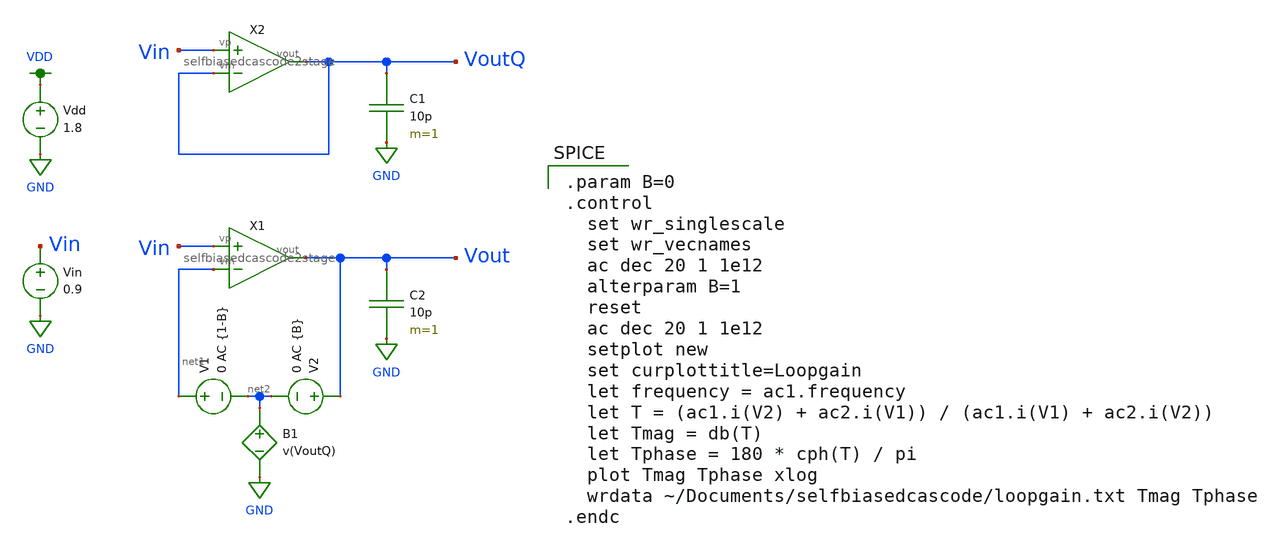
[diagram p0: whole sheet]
** sch_path: Final DAC files/schematics/opamp/selfbiasedcascode2stage_loopgain.sch
**.subckt selfbiasedcascode2stage_loopgain
Vdd VDD GND 1.8
Vin Vin GND 0.9
V1 net1 net2 0 AC {1-B}
V2 Vout net2 0 AC {B}
B1 net2 GND V=v(VoutQ)
X1 Vin net1 Vout selfbiasedcascode2stage
X2 Vin VoutQ VoutQ selfbiasedcascode2stage
C1 VoutQ GND 10p m=1
C2 Vout GND 10p m=1
**** begin user architecture code

.param B=0
.control
  set wr_singlescale
  set wr_vecnames
  ac dec 20 1 1e12
  alterparam B=1
  reset
  ac dec 20 1 1e12
  setplot new
  set curplottitle=Loopgain
  let frequency = ac1.frequency
  let T = (ac1.i(V2) + ac2.i(V1)) / (ac1.i(V1) + ac2.i(V2))
  let Tmag = db(T)
  let Tphase = 180 * cph(T) / pi
  plot Tmag Tphase xlog
  wrdata ~/Documents/selfbiasedcascode/loopgain.txt Tmag Tphase
.endc


.option wnflag=1
.param MC_SWITCH=0.0
.lib ~/skywater/skywater-pdk/libraries/sky130_fd_pr_ngspice/latest/models/sky130.lib.spice tt

**** end user architecture code
**.ends

* expanding   symbol:  /home/madvlsi/Documents/selfbiasedcascode/selfbiasedcascode2stage.sym # of
*+ pins=3
** sym_path: Final DAC files/schematics/opamp/selfbiasedcascode2stage.sym
** sch_path: Final DAC files/schematics/opamp/selfbiasedcascode2stage.sch
.subckt selfbiasedcascode2stage vp vm vout
*.ipin vp
*.ipin vm
*.opin vout
XM1 net11 net1 GND GND sky130_fd_pr__nfet_01v8 L=0.6 W=3 nf=1 ad='int((nf+1)/2) * W/nf * 0.29' as='int((nf+2)/2) * W/nf * 0.29'
+ pd='2*int((nf+1)/2) * (W/nf + 0.29)' ps='2*int((nf+2)/2) * (W/nf + 0.29)' nrd='0.29 / W' nrs='0.29 / W'
+ sa=0 sb=0 sd=0 mult=1 m=1
XM9 net12 net3 VDD VDD sky130_fd_pr__pfet_01v8 L=0.6 W=3 nf=1 ad='int((nf+1)/2) * W/nf * 0.29' as='int((nf+2)/2) * W/nf * 0.29'
+ pd='2*int((nf+1)/2) * (W/nf + 0.29)' ps='2*int((nf+2)/2) * (W/nf + 0.29)' nrd='0.29 / W' nrs='0.29 / W'
+ sa=0 sb=0 sd=0 mult=1 m=1
XM2 net5 net1 GND GND sky130_fd_pr__nfet_01v8 L=0.6 W=3 nf=1 ad='int((nf+1)/2) * W/nf * 0.29' as='int((nf+2)/2) * W/nf * 0.29'
+ pd='2*int((nf+1)/2) * (W/nf + 0.29)' ps='2*int((nf+2)/2) * (W/nf + 0.29)' nrd='0.29 / W' nrs='0.29 / W'
+ sa=0 sb=0 sd=0 mult=1 m=1
XM3 net6 net2 net11 GND sky130_fd_pr__nfet_01v8 L=0.6 W=3 nf=1 ad='int((nf+1)/2) * W/nf * 0.29' as='int((nf+2)/2) * W/nf * 0.29'
+ pd='2*int((nf+1)/2) * (W/nf + 0.29)' ps='2*int((nf+2)/2) * (W/nf + 0.29)' nrd='0.29 / W' nrs='0.29 / W'
+ sa=0 sb=0 sd=0 mult=1 m=1
XM4 net2 net2 net5 GND sky130_fd_pr__nfet_01v8 L=0.6 W=3 nf=1 ad='int((nf+1)/2) * W/nf * 0.29' as='int((nf+2)/2) * W/nf * 0.29'
+ pd='2*int((nf+1)/2) * (W/nf + 0.29)' ps='2*int((nf+2)/2) * (W/nf + 0.29)' nrd='0.29 / W' nrs='0.29 / W'
+ sa=0 sb=0 sd=0 mult=1 m=1
XM5 net1 net1 net5 GND sky130_fd_pr__nfet_01v8 L=0.6 W=3 nf=1 ad='int((nf+1)/2) * W/nf * 0.29' as='int((nf+2)/2) * W/nf * 0.29'
+ pd='2*int((nf+1)/2) * (W/nf + 0.29)' ps='2*int((nf+2)/2) * (W/nf + 0.29)' nrd='0.29 / W' nrs='0.29 / W'
+ sa=0 sb=0 sd=0 mult=1 m=1
XM6 net10 net1 GND GND sky130_fd_pr__nfet_01v8 L=0.6 W=3 nf=1 ad='int((nf+1)/2) * W/nf * 0.29' as='int((nf+2)/2) * W/nf * 0.29'
+ pd='2*int((nf+1)/2) * (W/nf + 0.29)' ps='2*int((nf+2)/2) * (W/nf + 0.29)' nrd='0.29 / W' nrs='0.29 / W'
+ sa=0 sb=0 sd=0 mult=1 m=1
XM7 net12 vp net10 GND sky130_fd_pr__nfet_01v8 L=0.6 W=3 nf=1 ad='int((nf+1)/2) * W/nf * 0.29' as='int((nf+2)/2) * W/nf * 0.29'
+ pd='2*int((nf+1)/2) * (W/nf + 0.29)' ps='2*int((nf+2)/2) * (W/nf + 0.29)' nrd='0.29 / W' nrs='0.29 / W'
+ sa=0 sb=0 sd=0 mult=1 m=1
XM8 net4 vm net10 GND sky130_fd_pr__nfet_01v8 L=0.6 W=3 nf=1 ad='int((nf+1)/2) * W/nf * 0.29' as='int((nf+2)/2) * W/nf * 0.29'
+ pd='2*int((nf+1)/2) * (W/nf + 0.29)' ps='2*int((nf+2)/2) * (W/nf + 0.29)' nrd='0.29 / W' nrs='0.29 / W'
+ sa=0 sb=0 sd=0 mult=1 m=1
XM10 net4 net3 VDD VDD sky130_fd_pr__pfet_01v8 L=0.6 W=3 nf=1 ad='int((nf+1)/2) * W/nf * 0.29' as='int((nf+2)/2) * W/nf * 0.29'
+ pd='2*int((nf+1)/2) * (W/nf + 0.29)' ps='2*int((nf+2)/2) * (W/nf + 0.29)' nrd='0.29 / W' nrs='0.29 / W'
+ sa=0 sb=0 sd=0 mult=1 m=1
XM11 net6 net2 net12 VDD sky130_fd_pr__pfet_01v8 L=0.6 W=3 nf=1 ad='int((nf+1)/2) * W/nf * 0.29' as='int((nf+2)/2) * W/nf * 0.29'
+ pd='2*int((nf+1)/2) * (W/nf + 0.29)' ps='2*int((nf+2)/2) * (W/nf + 0.29)' nrd='0.29 / W' nrs='0.29 / W'
+ sa=0 sb=0 sd=0 mult=1 m=1
XM12 net2 net2 net4 VDD sky130_fd_pr__pfet_01v8 L=0.6 W=3 nf=1 ad='int((nf+1)/2) * W/nf * 0.29' as='int((nf+2)/2) * W/nf * 0.29'
+ pd='2*int((nf+1)/2) * (W/nf + 0.29)' ps='2*int((nf+2)/2) * (W/nf + 0.29)' nrd='0.29 / W' nrs='0.29 / W'
+ sa=0 sb=0 sd=0 mult=1 m=1
XM13 net3 net3 net4 VDD sky130_fd_pr__pfet_01v8 L=0.6 W=3 nf=1 ad='int((nf+1)/2) * W/nf * 0.29' as='int((nf+2)/2) * W/nf * 0.29'
+ pd='2*int((nf+1)/2) * (W/nf + 0.29)' ps='2*int((nf+2)/2) * (W/nf + 0.29)' nrd='0.29 / W' nrs='0.29 / W'
+ sa=0 sb=0 sd=0 mult=1 m=1
XM14 net7 net3 VDD VDD sky130_fd_pr__pfet_01v8 L=0.6 W=3 nf=1 ad='int((nf+1)/2) * W/nf * 0.29' as='int((nf+2)/2) * W/nf * 0.29'
+ pd='2*int((nf+1)/2) * (W/nf + 0.29)' ps='2*int((nf+2)/2) * (W/nf + 0.29)' nrd='0.29 / W' nrs='0.29 / W'
+ sa=0 sb=0 sd=0 mult=1 m=1
XM15 net5 vm net7 VDD sky130_fd_pr__pfet_01v8 L=0.6 W=3 nf=1 ad='int((nf+1)/2) * W/nf * 0.29' as='int((nf+2)/2) * W/nf * 0.29'
+ pd='2*int((nf+1)/2) * (W/nf + 0.29)' ps='2*int((nf+2)/2) * (W/nf + 0.29)' nrd='0.29 / W' nrs='0.29 / W'
+ sa=0 sb=0 sd=0 mult=1 m=1
XM16 net11 vp net7 VDD sky130_fd_pr__pfet_01v8 L=0.6 W=3 nf=1 ad='int((nf+1)/2) * W/nf * 0.29' as='int((nf+2)/2) * W/nf * 0.29'
+ pd='2*int((nf+1)/2) * (W/nf + 0.29)' ps='2*int((nf+2)/2) * (W/nf + 0.29)' nrd='0.29 / W' nrs='0.29 / W'
+ sa=0 sb=0 sd=0 mult=1 m=1
XM17 net8 net1 GND GND sky130_fd_pr__nfet_01v8 L=0.6 W=3 nf=1 ad='int((nf+1)/2) * W/nf * 0.29' as='int((nf+2)/2) * W/nf * 0.29'
+ pd='2*int((nf+1)/2) * (W/nf + 0.29)' ps='2*int((nf+2)/2) * (W/nf + 0.29)' nrd='0.29 / W' nrs='0.29 / W'
+ sa=0 sb=0 sd=0 mult=1 m=1
XM18 net3 net1 net8 GND sky130_fd_pr__nfet_01v8 L=0.6 W=3 nf=1 ad='int((nf+1)/2) * W/nf * 0.29' as='int((nf+2)/2) * W/nf * 0.29'
+ pd='2*int((nf+1)/2) * (W/nf + 0.29)' ps='2*int((nf+2)/2) * (W/nf + 0.29)' nrd='0.29 / W' nrs='0.29 / W'
+ sa=0 sb=0 sd=0 mult=1 m=1
XM19 VDD net1 net8 GND sky130_fd_pr__nfet_01v8 L=0.6 W=3 nf=1 ad='int((nf+1)/2) * W/nf * 0.29' as='int((nf+2)/2) * W/nf * 0.29'
+ pd='2*int((nf+1)/2) * (W/nf + 0.29)' ps='2*int((nf+2)/2) * (W/nf + 0.29)' nrd='0.29 / W' nrs='0.29 / W'
+ sa=0 sb=0 sd=0 mult=3 m=3
XM20 net1 net3 net9 VDD sky130_fd_pr__pfet_01v8 L=0.6 W=3 nf=1 ad='int((nf+1)/2) * W/nf * 0.29' as='int((nf+2)/2) * W/nf * 0.29'
+ pd='2*int((nf+1)/2) * (W/nf + 0.29)' ps='2*int((nf+2)/2) * (W/nf + 0.29)' nrd='0.29 / W' nrs='0.29 / W'
+ sa=0 sb=0 sd=0 mult=1 m=1
XM21 net9 net3 VDD VDD sky130_fd_pr__pfet_01v8 L=0.6 W=3 nf=1 ad='int((nf+1)/2) * W/nf * 0.29' as='int((nf+2)/2) * W/nf * 0.29'
+ pd='2*int((nf+1)/2) * (W/nf + 0.29)' ps='2*int((nf+2)/2) * (W/nf + 0.29)' nrd='0.29 / W' nrs='0.29 / W'
+ sa=0 sb=0 sd=0 mult=1 m=1
XM22 GND net3 net9 VDD sky130_fd_pr__pfet_01v8 L=0.6 W=3 nf=1 ad='int((nf+1)/2) * W/nf * 0.29' as='int((nf+2)/2) * W/nf * 0.29'
+ pd='2*int((nf+1)/2) * (W/nf + 0.29)' ps='2*int((nf+2)/2) * (W/nf + 0.29)' nrd='0.29 / W' nrs='0.29 / W'
+ sa=0 sb=0 sd=0 mult=3 m=3
XM23 vout net6 VDD VDD sky130_fd_pr__pfet_01v8 L=0.15 W=12 nf=1 ad='int((nf+1)/2) * W/nf * 0.29' as='int((nf+2)/2) * W/nf * 0.29'
+ pd='2*int((nf+1)/2) * (W/nf + 0.29)' ps='2*int((nf+2)/2) * (W/nf + 0.29)' nrd='0.29 / W' nrs='0.29 / W'
+ sa=0 sb=0 sd=0 mult=1 m=1
XM24 vout net6 GND GND sky130_fd_pr__nfet_01v8 L=0.15 W=6 nf=1 ad='int((nf+1)/2) * W/nf * 0.29' as='int((nf+2)/2) * W/nf * 0.29'
+ pd='2*int((nf+1)/2) * (W/nf + 0.29)' ps='2*int((nf+2)/2) * (W/nf + 0.29)' nrd='0.29 / W' nrs='0.29 / W'
+ sa=0 sb=0 sd=0 mult=1 m=1
C1 net6 vout 500f m=1
.ends

.GLOBAL GND
.GLOBAL VDD
.end
